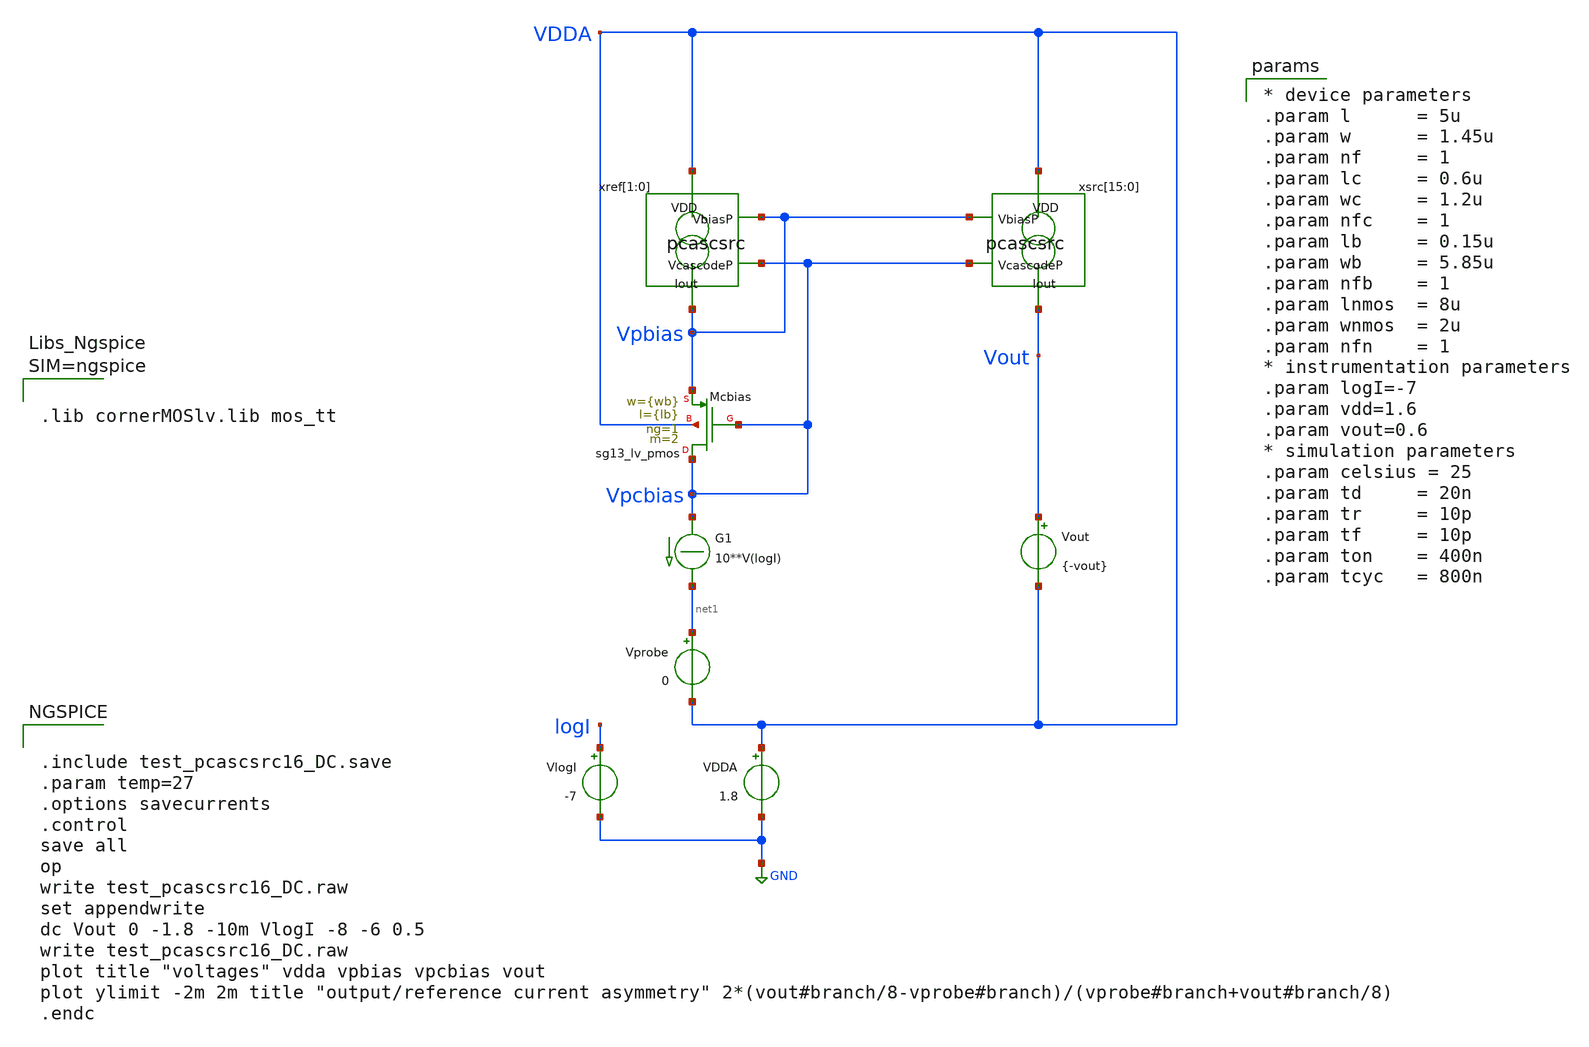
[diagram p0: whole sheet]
** sch_path: xschem/test_pcascsrc16_DC.sch
**.subckt test_pcascsrc16_DC
Vout Vout VDDA {-vout}
.save i(vout)
Vprobe net1 VDDA 0
.save i(vprobe)
G1 Vpcbias net1 CUR=' 10**V(logI) '
VlogI logI GND -7
.save i(vlogi)
xref[1] VDDA Vpbias Vpcbias Vpbias pcascsrc l={l} w={w} lc={lc} wc={wc}
xref[0] VDDA Vpbias Vpcbias Vpbias pcascsrc l={l} w={w} lc={lc} wc={wc}
xsrc[15] VDDA Vpbias Vpcbias Vout pcascsrc l={l} w={w} lc={lc} wc={wc}
xsrc[14] VDDA Vpbias Vpcbias Vout pcascsrc l={l} w={w} lc={lc} wc={wc}
xsrc[13] VDDA Vpbias Vpcbias Vout pcascsrc l={l} w={w} lc={lc} wc={wc}
xsrc[12] VDDA Vpbias Vpcbias Vout pcascsrc l={l} w={w} lc={lc} wc={wc}
xsrc[11] VDDA Vpbias Vpcbias Vout pcascsrc l={l} w={w} lc={lc} wc={wc}
xsrc[10] VDDA Vpbias Vpcbias Vout pcascsrc l={l} w={w} lc={lc} wc={wc}
xsrc[9] VDDA Vpbias Vpcbias Vout pcascsrc l={l} w={w} lc={lc} wc={wc}
xsrc[8] VDDA Vpbias Vpcbias Vout pcascsrc l={l} w={w} lc={lc} wc={wc}
xsrc[7] VDDA Vpbias Vpcbias Vout pcascsrc l={l} w={w} lc={lc} wc={wc}
xsrc[6] VDDA Vpbias Vpcbias Vout pcascsrc l={l} w={w} lc={lc} wc={wc}
xsrc[5] VDDA Vpbias Vpcbias Vout pcascsrc l={l} w={w} lc={lc} wc={wc}
xsrc[4] VDDA Vpbias Vpcbias Vout pcascsrc l={l} w={w} lc={lc} wc={wc}
xsrc[3] VDDA Vpbias Vpcbias Vout pcascsrc l={l} w={w} lc={lc} wc={wc}
xsrc[2] VDDA Vpbias Vpcbias Vout pcascsrc l={l} w={w} lc={lc} wc={wc}
xsrc[1] VDDA Vpbias Vpcbias Vout pcascsrc l={l} w={w} lc={lc} wc={wc}
xsrc[0] VDDA Vpbias Vpcbias Vout pcascsrc l={l} w={w} lc={lc} wc={wc}
VDDA VDDA GND 1.8
.save i(vdda)
XMcbias Vpcbias Vpcbias Vpbias VDDA sg13_lv_pmos w={wb} l={lb} ng=1 m=2 mm_ok=1
**** begin user architecture code


.include test_pcascsrc16_DC.save
.param temp=27
.options savecurrents
.control
save all
op
write test_pcascsrc16_DC.raw
set appendwrite
dc Vout 0 -1.8 -10m VlogI -8 -6 0.5
write test_pcascsrc16_DC.raw
plot title "voltages" vdda vpbias vpcbias vout
plot ylimit -2m 2m title "output/reference current asymmetry"
+ 2*(vout#branch/8-vprobe#branch)/(vprobe#branch+vout#branch/8)
.endc





.lib cornerMOSlv.lib mos_tt




* device parameters
.param l      = 5u
.param w      = 1.45u
.param nf     = 1
.param lc     = 0.6u
.param wc     = 1.2u
.param nfc    = 1
.param lb     = 0.15u
.param wb     = 5.85u
.param nfb    = 1
.param lnmos  = 8u
.param wnmos  = 2u
.param nfn    = 1
* instrumentation parameters
.param logI=-7
.param vdd=1.6
.param vout=0.6
* simulation parameters
.param celsius = 25
.param td     = 20n
.param tr     = 10p
.param tf     = 10p
.param ton    = 400n
.param tcyc   = 800n


**** end user architecture code
**.ends

* expanding   symbol:  pcascsrc.sym # of pins=4
** sym_path: xschem/pcascsrc.sym
** sch_path: xschem/pcascsrc.sch
.subckt pcascsrc VDD VbiasP VcascodeP Iout  l=2u w=.74u lc=.3u wc=.3u
*.ipin VcascodeP
*.ipin VbiasP
*.opin Iout
*.ipin VDD
XMsrc drain VbiasP VDD VDD sg13_lv_pmos w={w} l={l} ng=1 m=1 mm_ok=1
XMcasc Iout VcascodeP drain VDD sg13_lv_pmos w={wc} l={lc} ng=1 m=1 mm_ok=1
.ends

.GLOBAL GND
.end
